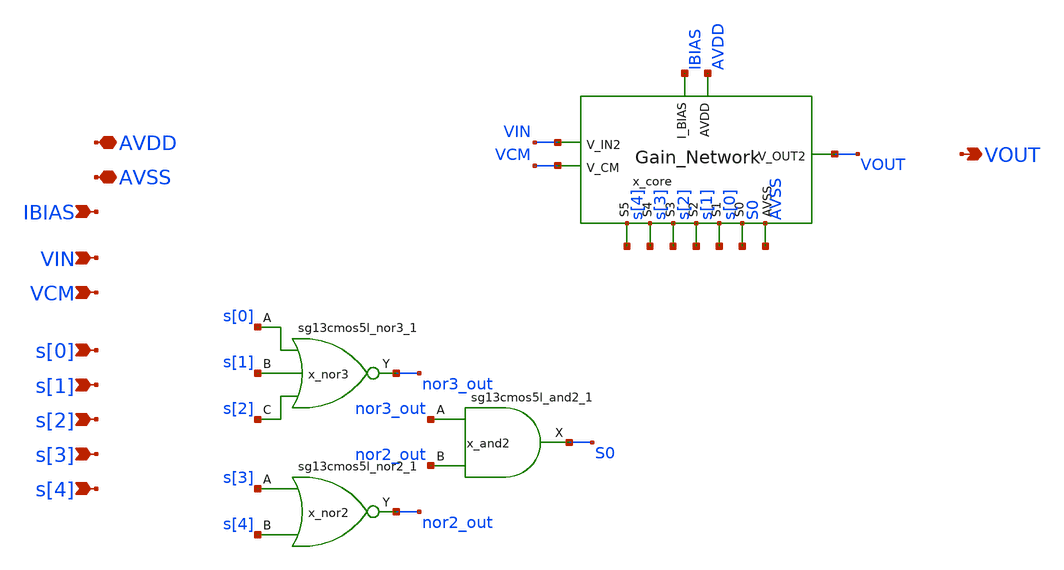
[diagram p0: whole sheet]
** sch_path: xschem/gain_stage/gain_stage.sch
**.subckt gain_stage AVDD AVSS IBIAS VIN VCM VOUT s[0] s[1] s[2] s[3] s[4]
*.iopin AVDD
*.iopin AVSS
*.ipin IBIAS
*.ipin VIN
*.ipin VCM
*.opin VOUT
*.ipin s[0]
*.ipin s[1]
*.ipin s[2]
*.ipin s[3]
*.ipin s[4]
x_nor3 nor3_out s[0] s[1] s[2] AVDD AVSS sg13cmos5l_nor3_1
x_nor2 nor2_out s[3] s[4] AVDD AVSS sg13cmos5l_nor2_1
x_and2 S0 nor3_out nor2_out AVDD AVSS sg13cmos5l_and2_1
x_core s[3] s[4] S0 s[1] s[0] s[2] AVDD VCM VIN VOUT IBIAS AVSS gain_network
**.ends
.end
